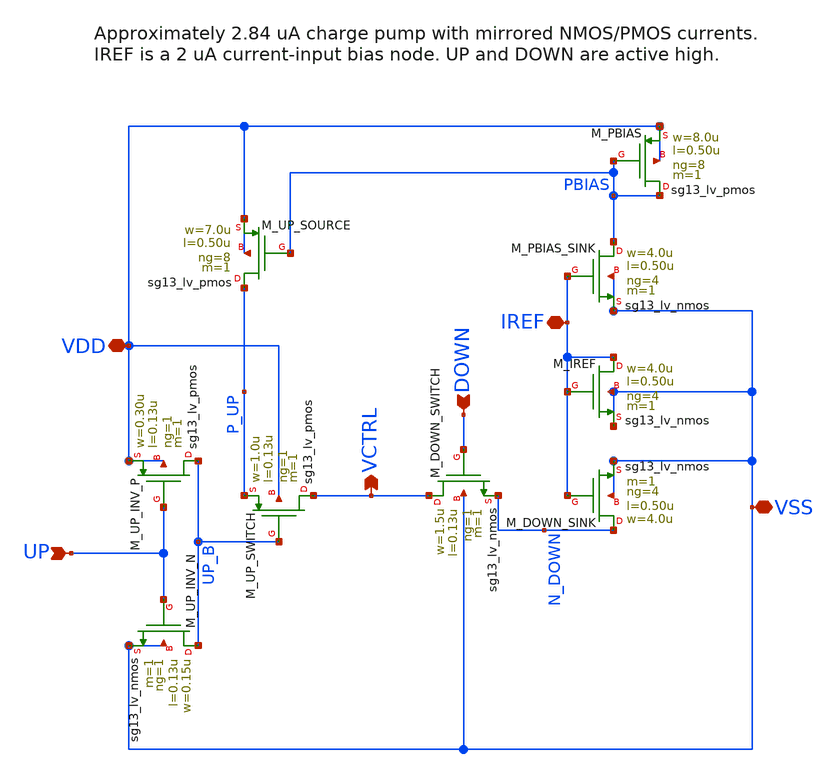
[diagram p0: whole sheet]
** sch_path: macros/pll_analog/schematic/xschem/charge_pump.sch
**.subckt charge_pump UP DOWN IREF VCTRL VDD VSS
*.ipin UP
*.ipin DOWN
*.iopin IREF
*.opin VCTRL
*.iopin VDD
*.iopin VSS
XM_UP_INV_P UP_B UP VDD VDD sg13_lv_pmos w=0.30u l=0.13u ng=1 m=1 mm_ok=1
XM_UP_INV_N UP_B UP VSS VSS sg13_lv_nmos w=0.15u l=0.13u ng=1 m=1 mm_ok=1
XM_IREF IREF IREF VSS VSS sg13_lv_nmos w=4.0u l=0.50u ng=4 m=1 mm_ok=1
XM_PBIAS PBIAS PBIAS VDD VDD sg13_lv_pmos w=8.0u l=0.50u ng=8 m=1 mm_ok=1
XM_PBIAS_SINK PBIAS IREF VSS VSS sg13_lv_nmos w=4.0u l=0.50u ng=4 m=1 mm_ok=1
XM_UP_SOURCE P_UP PBIAS VDD VDD sg13_lv_pmos w=7.0u l=0.50u ng=8 m=1 mm_ok=1
XM_UP_SWITCH VCTRL UP_B P_UP VDD sg13_lv_pmos w=1.0u l=0.13u ng=1 m=1 mm_ok=1
XM_DOWN_SWITCH VCTRL DOWN N_DOWN VSS sg13_lv_nmos w=1.5u l=0.13u ng=1 m=1 mm_ok=1
XM_DOWN_SINK N_DOWN IREF VSS VSS sg13_lv_nmos w=4.0u l=0.50u ng=4 m=1 mm_ok=1
**.ends
.end
